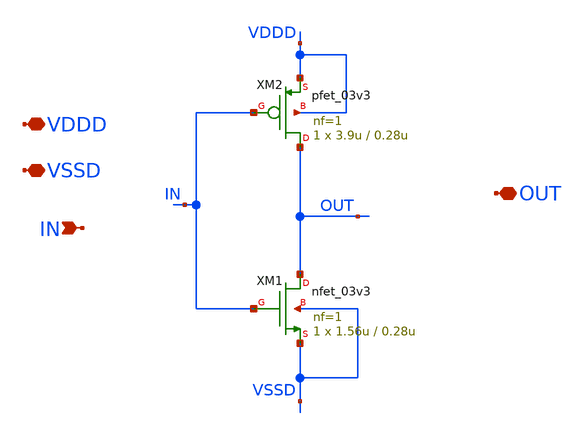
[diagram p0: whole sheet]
** sch_path: SAR_ADC/SAR_Asynchronous_Logic/xschem/SAR_Asynchronous_Logic_inv_1x.sch
**.subckt SAR_Asynchronous_Logic_inv_1x VDDD VSSD OUT IN
*.iopin VDDD
*.iopin VSSD
*.iopin OUT
*.ipin IN
XM1 OUT IN VSSD VSSD nfet_03v3 L=0.28u W=1.56u nf=1 ad='int((nf+1)/2) * W/nf * 0.18u' as='int((nf+2)/2) * W/nf * 0.18u'
+ pd='2*int((nf+1)/2) * (W/nf + 0.18u)' ps='2*int((nf+2)/2) * (W/nf + 0.18u)' nrd='0.18u / W' nrs='0.18u / W'
+ sa=0 sb=0 sd=0 m=1
XM2 OUT IN VDDD VDDD pfet_03v3 L=0.28u W=3.9u nf=1 ad='int((nf+1)/2) * W/nf * 0.18u' as='int((nf+2)/2) * W/nf * 0.18u'
+ pd='2*int((nf+1)/2) * (W/nf + 0.18u)' ps='2*int((nf+2)/2) * (W/nf + 0.18u)' nrd='0.18u / W' nrs='0.18u / W'
+ sa=0 sb=0 sd=0 m=1
**.ends
.end
